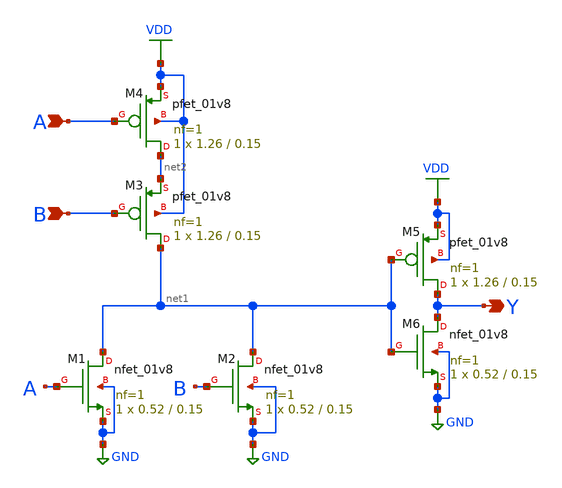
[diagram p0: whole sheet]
** sch_path: xschem/or21.sch
**.subckt or21 B A Y
*.ipin B
*.ipin A
*.opin Y
XM1 net1 A GND GND sky130_fd_pr__nfet_01v8 L=0.15 W=0.52 nf=1 ad='int((nf+1)/2) * W/nf * 0.29' as='int((nf+2)/2) * W/nf * 0.29'
+ pd='2*int((nf+1)/2) * (W/nf + 0.29)' ps='2*int((nf+2)/2) * (W/nf + 0.29)' nrd='0.29 / W' nrs='0.29 / W'
+ sa=0 sb=0 sd=0 mult=1 m=1
XM2 net1 B GND GND sky130_fd_pr__nfet_01v8 L=0.15 W=0.52 nf=1 ad='int((nf+1)/2) * W/nf * 0.29' as='int((nf+2)/2) * W/nf * 0.29'
+ pd='2*int((nf+1)/2) * (W/nf + 0.29)' ps='2*int((nf+2)/2) * (W/nf + 0.29)' nrd='0.29 / W' nrs='0.29 / W'
+ sa=0 sb=0 sd=0 mult=1 m=1
XM3 net1 B net2 VDD sky130_fd_pr__pfet_01v8 L=0.15 W=1.26 nf=1 ad='int((nf+1)/2) * W/nf * 0.29' as='int((nf+2)/2) * W/nf * 0.29'
+ pd='2*int((nf+1)/2) * (W/nf + 0.29)' ps='2*int((nf+2)/2) * (W/nf + 0.29)' nrd='0.29 / W' nrs='0.29 / W'
+ sa=0 sb=0 sd=0 mult=1 m=1
XM4 net2 A VDD VDD sky130_fd_pr__pfet_01v8 L=0.15 W=1.26 nf=1 ad='int((nf+1)/2) * W/nf * 0.29' as='int((nf+2)/2) * W/nf * 0.29'
+ pd='2*int((nf+1)/2) * (W/nf + 0.29)' ps='2*int((nf+2)/2) * (W/nf + 0.29)' nrd='0.29 / W' nrs='0.29 / W'
+ sa=0 sb=0 sd=0 mult=1 m=1
XM5 Y net1 VDD VDD sky130_fd_pr__pfet_01v8 L=0.15 W=1.26 nf=1 ad='int((nf+1)/2) * W/nf * 0.29' as='int((nf+2)/2) * W/nf * 0.29'
+ pd='2*int((nf+1)/2) * (W/nf + 0.29)' ps='2*int((nf+2)/2) * (W/nf + 0.29)' nrd='0.29 / W' nrs='0.29 / W'
+ sa=0 sb=0 sd=0 mult=1 m=1
XM6 Y net1 GND GND sky130_fd_pr__nfet_01v8 L=0.15 W=0.52 nf=1 ad='int((nf+1)/2) * W/nf * 0.29' as='int((nf+2)/2) * W/nf * 0.29'
+ pd='2*int((nf+1)/2) * (W/nf + 0.29)' ps='2*int((nf+2)/2) * (W/nf + 0.29)' nrd='0.29 / W' nrs='0.29 / W'
+ sa=0 sb=0 sd=0 mult=1 m=1
**.ends
.GLOBAL GND
.GLOBAL VDD
.end
